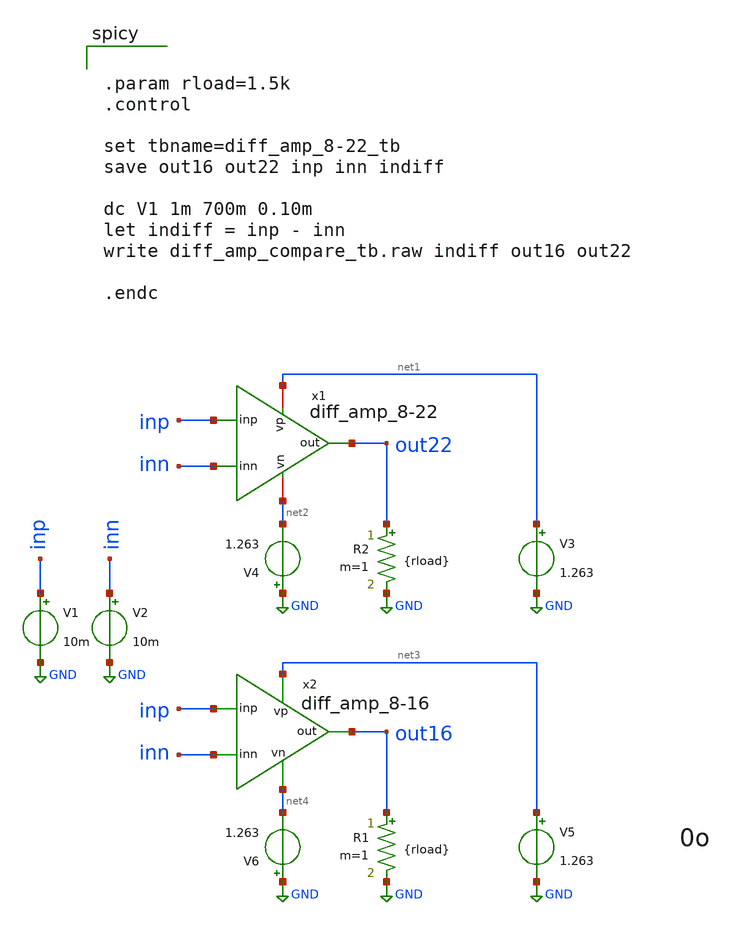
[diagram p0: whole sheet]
** sch_path: TempSensor/design_data/xschem/diff_amp_compare_tb.sch
**.subckt diff_amp_compare_tb
V2 inn GND 10m
V1 inp GND 10m
V3 net1 GND 1.263
x1 net1 out22 inp inn net2 diff_amp_8-22
R2 out22 GND {rload} m=1
V4 GND net2 1.263
x2 net3 inn inp out16 net4 diff_amp_8-16
V5 net3 GND 1.263
R1 out16 GND {rload} m=1
V6 GND net4 1.263
**** begin user architecture code


** IHP models
.lib cornerMOSlv.lib mos_tt
.lib cornerCAP.lib cap_typ
.lib cornerRES.lib res_typ




.param rload=1.5k
.control

set tbname=diff_amp_8-22_tb
save out16 out22 inp inn indiff

dc V1 1m 700m 0.10m
let indiff = inp - inn
write diff_amp_compare_tb.raw indiff out16 out22

.endc


**** end user architecture code
**.ends

* expanding   symbol:  practicing/TempSensor/design_data/xschem/diff_amp_8-22.sym # of pins=5
** sym_path: TempSensor/design_data/xschem/diff_amp_8-22.sym
** sch_path: TempSensor/design_data/xschem/diff_amp_8-22.sch
.subckt diff_amp_8-22 vp out inp inn vn
*.opin out
*.iopin vn
*.iopin vp
*.ipin inp
*.ipin inn
XM5 net18 net1 vp vp sg13_lv_pmos w=10u l=3.33u ng=1 m=1 mm_ok=1
XM30 net15 inn net6 vn sg13_lv_nmos w=10u l=1.5u ng=1 m=5 mm_ok=1
I0 vp net4 5u
XM7 net19 net1 vp vp sg13_lv_pmos w=10u l=3.33u ng=1 m=2 mm_ok=1
XM6 net1 net1 net18 vp sg13_lv_pmos w=10u l=1u ng=1 m=1 mm_ok=1
XM8 net5 net1 net19 vp sg13_lv_pmos w=10u l=.5u ng=1 m=1 mm_ok=1
XM11 net15 net7 vp vp sg13_lv_pmos w=10u l=2.5u ng=1 m=5 mm_ok=1
XM13 net16 net7 vp vp sg13_lv_pmos w=10u l=2.5u ng=1 m=5 mm_ok=1
XM12 net7 net7 net15 vp sg13_lv_pmos w=10u l=1u ng=1 m=5 mm_ok=1
XM14 out net7 net16 vp sg13_lv_pmos w=10u l=1u ng=1 m=5 mm_ok=1
XM21 net12 net12 vp vp sg13_lv_pmos w=10u l=.33u ng=1 m=10 mm_ok=1
XM24 net13 net1 vp vp sg13_lv_pmos w=4u l=5u ng=1 m=1 mm_ok=1
XM22 net11 net11 net12 vp sg13_lv_pmos w=10u l=.33u ng=1 m=10 mm_ok=1
XM29 vp inp net6 vn sg13_lv_nmos w=10u l=1.5u ng=1 m=5 mm_ok=1
XM9 net9 inp net5 net5 sg13_lv_pmos w=10u l=1.5u ng=1 m=10 mm_ok=1
XM10 net8 inn net5 net5 sg13_lv_pmos w=10u l=1.5u ng=1 m=10 mm_ok=1
XM1 net4 net4 net3 vn sg13_lv_nmos w=10u l=2u ng=1 m=1 mm_ok=1
XM2 net3 net4 vn vn sg13_lv_nmos w=5u l=5u ng=1 m=1 mm_ok=1
XM3 net1 net4 net2 vn sg13_lv_nmos w=10u l=2u ng=1 m=1 mm_ok=1
XM4 net2 net4 vn vn sg13_lv_nmos w=5u l=5u ng=1 m=1 mm_ok=1
XM31 net6 net4 net17 vn sg13_lv_nmos w=10u l=1u ng=1 m=1 mm_ok=1
XM32 net17 net4 vn vn sg13_lv_nmos w=10u l=5u ng=1 m=1 mm_ok=1
XM15 net7 net4 net8 vn sg13_lv_nmos w=10u l=1u ng=1 m=5 mm_ok=1
XM16 net8 net4 vn vn sg13_lv_nmos w=10u l=5u ng=1 m=1 mm_ok=1
XM17 net10 net4 net9 vn sg13_lv_nmos w=10u l=1u ng=1 m=5 mm_ok=1
XM18 net9 net4 vn vn sg13_lv_nmos w=10u l=5u ng=1 m=1 mm_ok=1
XM20 net11 net4 vn vn sg13_lv_nmos w=1.5u l=5u ng=1 m=1 mm_ok=1
XM19 net10 net11 out vp sg13_lv_pmos w=10u l=.33u ng=1 m=10 mm_ok=1
XM23 out net13 net10 vn sg13_lv_nmos w=10u l=.5u ng=1 m=5 mm_ok=1
XM25 net13 net13 net14 vn sg13_lv_nmos w=10u l=.5u ng=1 m=5 mm_ok=1
XM26 net14 net14 vn vn sg13_lv_nmos w=10u l=.5u ng=1 m=5 mm_ok=1
XM27 vp out out vp sg13_lv_nmos w=10u l=.33u ng=1 m=10 mm_ok=1
XM28 vn net10 out vn sg13_lv_pmos w=10u l=.5u ng=1 m=5 mm_ok=1
XC1 out out cap_cmim w=3.5e-5 l=3.5e-5 m=1 mm_ok=1
XC2 out net10 cap_cmim w=3.5e-5 l=3.5e-5 m=1 mm_ok=1
.ends


* expanding   symbol:  practicing/TempSensor/design_data/xschem/diff_amp_8-16.sym # of pins=5
** sym_path: TempSensor/design_data/xschem/diff_amp_8-16.sym
** sch_path: TempSensor/design_data/xschem/diff_amp_8-16.sch
.subckt diff_amp_8-16 vp inn inp out vn
*.ipin inp
*.opin out
*.ipin inn
*.iopin vn
*.iopin vp
XM6 net10 inn net2 vn sg13_lv_nmos w=10u l=0.5u ng=1 m=1 mm_ok=1
XM5 net11 inp net2 vn sg13_lv_nmos w=10u l=0.5u ng=1 m=1 mm_ok=1
XM2 net1 net1 net4 vp sg13_lv_pmos w=10u l=2u ng=1 m=10 mm_ok=1
XM1 net4 net1 vp vp sg13_lv_pmos w=6u l=1u ng=1 m=1 mm_ok=1
XM3 net3 net1 vp vp sg13_lv_pmos w=6u l=1u ng=1 m=1 mm_ok=1
XM4 net5 net1 net3 vp sg13_lv_pmos w=10u l=2u ng=1 m=10 mm_ok=1
XM7 net5 net5 net6 vn sg13_lv_nmos w=10u l=2u ng=1 m=10 mm_ok=1
XM8 net6 net5 vn vn sg13_lv_nmos w=10u l=5u ng=1 m=1 mm_ok=1
XM9 net2 net5 net7 vn sg13_lv_nmos w=10u l=2u ng=1 m=10 mm_ok=1
XM10 net7 net5 vn vn sg13_lv_nmos w=10u l=5u ng=1 m=1 mm_ok=1
XM15 net8 net8 vn vn sg13_lv_nmos w=10u l=1.5u ng=1 m=1 mm_ok=1
XM16 net9 net8 vn vn sg13_lv_nmos w=10u l=1.5u ng=1 m=1 mm_ok=1
XM11 net10 net1 vp vp sg13_lv_pmos w=10u l=1.67u ng=1 m=1 mm_ok=1
XM12 net8 net1 net10 vp sg13_lv_pmos w=10u l=2u ng=1 m=10 mm_ok=1
XM13 net11 net1 vp vp sg13_lv_pmos w=10u l=1.67u ng=1 m=1 mm_ok=1
XM14 net9 net1 net11 vp sg13_lv_pmos w=10u l=2u ng=1 m=10 mm_ok=1
XM17 out net1 vp vp sg13_lv_pmos w=9u l=5u ng=1 m=10 mm_ok=1
XM18 out net9 vn vn sg13_lv_nmos w=10u l=0.5u ng=1 m=5 mm_ok=1
I0 net1 vn 20u
XC2 out net9 cap_cmim w=35e-6 l=35e-6 m=1 mm_ok=1
.ends

.GLOBAL GND
.end
